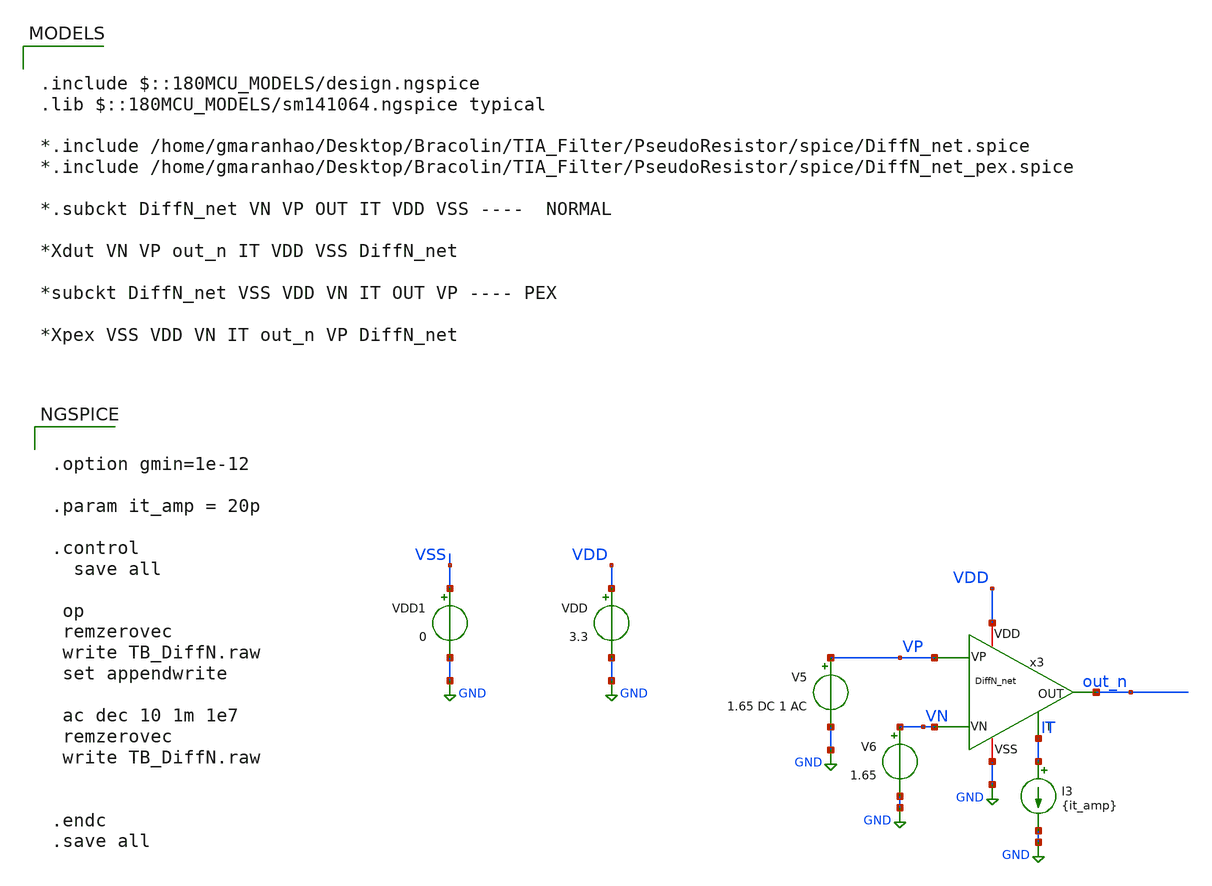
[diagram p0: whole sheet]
** sch_path: TIA_Filter/PseudoResistor/TB_DiffN.sch
**.subckt TB_DiffN
VDD VDD GND 3.3
x3 VN VP out_n IT VDD GND DiffN_net
V5 VP GND 1.65 DC 1 AC
V6 VN GND 1.65
I3 IT GND {it_amp}
VDD1 VSS GND 0
**** begin user architecture code

.include $::180MCU_MODELS/design.ngspice
.lib $::180MCU_MODELS/sm141064.ngspice typical

*.include /home/gmaranhao/Desktop/Bracolin/TIA_Filter/PseudoResistor/spice/DiffN_net.spice
*.include /home/gmaranhao/Desktop/Bracolin/TIA_Filter/PseudoResistor/spice/DiffN_net_pex.spice

*.subckt DiffN_net VN VP OUT IT VDD VSS ----  NORMAL

*Xdut VN VP out_n IT VDD VSS DiffN_net

*subckt DiffN_net VSS VDD VN IT OUT VP ---- PEX

*Xpex VSS VDD VN IT out_n VP DiffN_net




.option gmin=1e-12

.param it_amp = 20p

.control
  save all

 op
 remzerovec
 write TB_DiffN.raw
 set appendwrite

 ac dec 10 1m 1e7
 remzerovec
 write TB_DiffN.raw


.endc
.save all


**** end user architecture code
**.ends
.GLOBAL GND
.end
